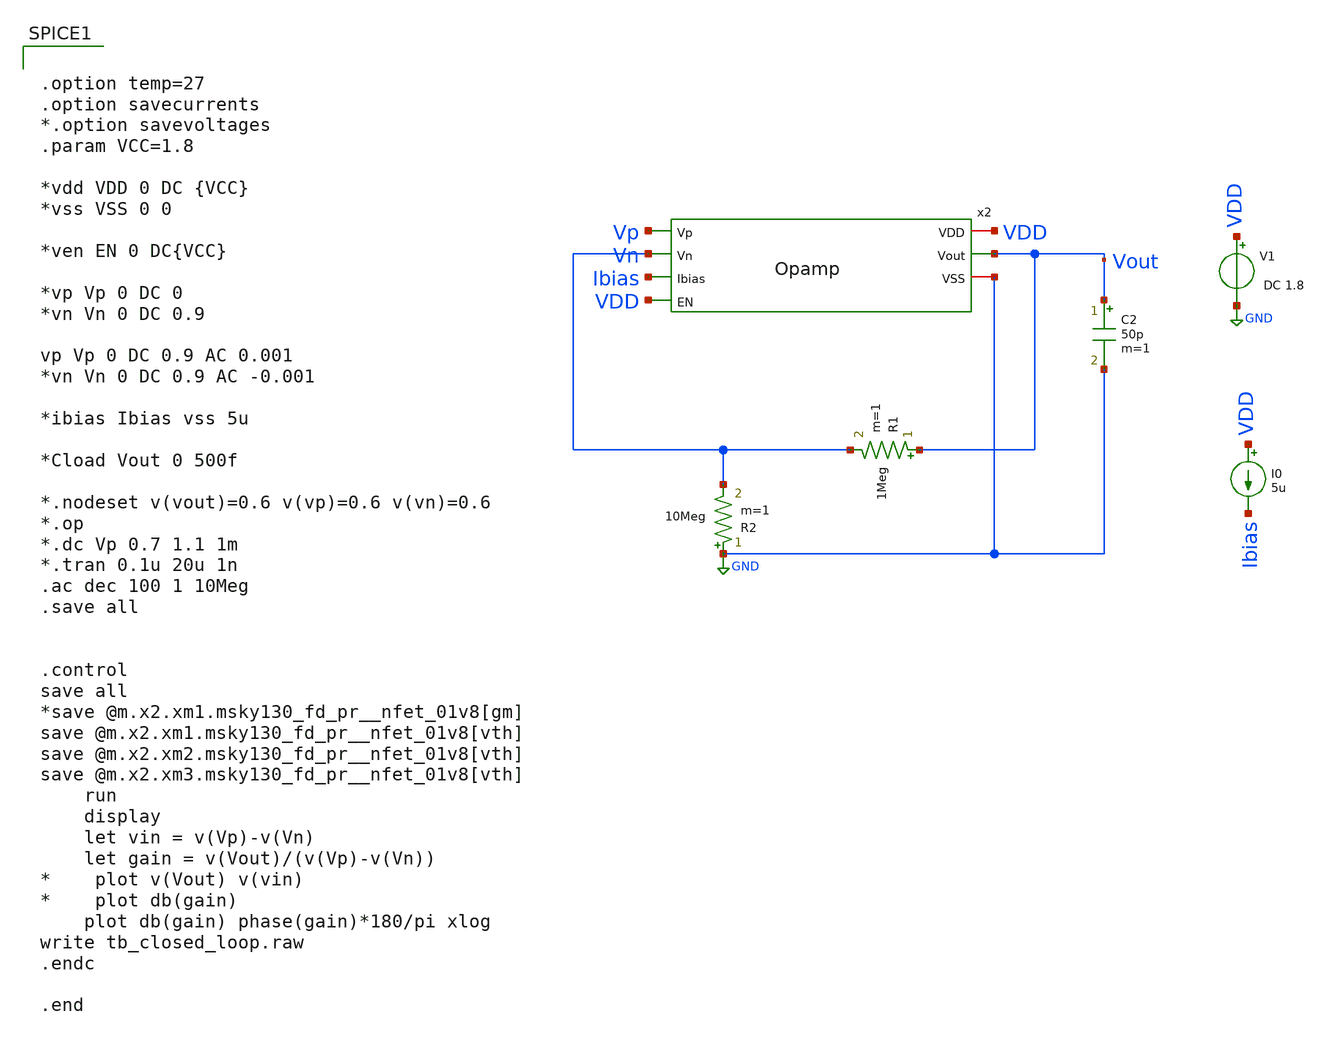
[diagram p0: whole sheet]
** sch_path: xschem/tb_closed_loop.sch
**.subckt tb_closed_loop
R1 Vout Vn 1Meg m=1
V1 VDD GND DC 1.8
I0 VDD Ibias 5u
x2 VDD Vp Vn Vout Ibias GND VDD Opamp
C2 Vout GND 50p m=1
R2 GND Vn 10Meg m=1
**** begin user architecture code


.option temp=27
.option savecurrents
*.option savevoltages
.param VCC=1.8

*vdd VDD 0 DC {VCC}
*vss VSS 0 0

*ven EN 0 DC{VCC}

*vp Vp 0 DC 0
*vn Vn 0 DC 0.9

vp Vp 0 DC 0.9 AC 0.001
*vn Vn 0 DC 0.9 AC -0.001

*ibias Ibias vss 5u

*Cload Vout 0 500f

*.nodeset v(vout)=0.6 v(vp)=0.6 v(vn)=0.6
*.op
*.dc Vp 0.7 1.1 1m
*.tran 0.1u 20u 1n
.ac dec 100 1 10Meg
.save all


.control
save all
*save @m.x2.xm1.msky130_fd_pr__nfet_01v8[gm]
save @m.x2.xm1.msky130_fd_pr__nfet_01v8[vth]
save @m.x2.xm2.msky130_fd_pr__nfet_01v8[vth]
save @m.x2.xm3.msky130_fd_pr__nfet_01v8[vth]
	run
	display
	let vin = v(Vp)-v(Vn)
	let gain = v(Vout)/(v(Vp)-v(Vn))
*	plot v(Vout) v(vin)
*	plot db(gain)
	plot db(gain) phase(gain)*180/pi xlog
write tb_closed_loop.raw
.endc

.end



** opencircuitdesign pdks install
.lib /foss/pdks/sky130A/libs.tech/ngspice/sky130.lib.spice tt


**** end user architecture code
**.ends

* expanding   symbol:  /foss/designs/cmos-two-stage-opamp/xschem/Opamp.sym # of pins=7
** sym_path: xschem/Opamp.sym
** sch_path: xschem/Opamp.sch
.subckt Opamp VDD Vp Vn Vout Ibias VSS EN
*.ipin Vn
*.ipin Ibias
*.ipin Vp
*.ipin EN
*.opin Vout
*.iopin VSS
*.iopin VDD
XM2 Vouts1 Vp Itail GND sky130_fd_pr__nfet_01v8 L=1 W=4 nf=1 ad='int((nf+1)/2) * W/nf * 0.29' as='int((nf+2)/2) * W/nf * 0.29'
+ pd='2*int((nf+1)/2) * (W/nf + 0.29)' ps='2*int((nf+2)/2) * (W/nf + 0.29)' nrd='0.29 / W' nrs='0.29 / W'
+ sa=0 sb=0 sd=0 mult=1 m=1
XM4 Vouts1 net1 VDD VDD sky130_fd_pr__pfet_01v8 L=1 W=8 nf=1 ad='int((nf+1)/2) * W/nf * 0.29' as='int((nf+2)/2) * W/nf * 0.29'
+ pd='2*int((nf+1)/2) * (W/nf + 0.29)' ps='2*int((nf+2)/2) * (W/nf + 0.29)' nrd='0.29 / W' nrs='0.29 / W'
+ sa=0 sb=0 sd=0 mult=1 m=1
XM3 net1 net1 VDD VDD sky130_fd_pr__pfet_01v8 L=1 W=8 nf=1 ad='int((nf+1)/2) * W/nf * 0.29' as='int((nf+2)/2) * W/nf * 0.29'
+ pd='2*int((nf+1)/2) * (W/nf + 0.29)' ps='2*int((nf+2)/2) * (W/nf + 0.29)' nrd='0.29 / W' nrs='0.29 / W'
+ sa=0 sb=0 sd=0 mult=1 m=1
XM1 net1 Vn Itail GND sky130_fd_pr__nfet_01v8 L=1 W=4 nf=1 ad='int((nf+1)/2) * W/nf * 0.29' as='int((nf+2)/2) * W/nf * 0.29'
+ pd='2*int((nf+1)/2) * (W/nf + 0.29)' ps='2*int((nf+2)/2) * (W/nf + 0.29)' nrd='0.29 / W' nrs='0.29 / W'
+ sa=0 sb=0 sd=0 mult=1 m=1
XM6 Vout Vouts1 VDD VDD sky130_fd_pr__pfet_01v8 L=1 W=22 nf=1 ad='int((nf+1)/2) * W/nf * 0.29' as='int((nf+2)/2) * W/nf * 0.29'
+ pd='2*int((nf+1)/2) * (W/nf + 0.29)' ps='2*int((nf+2)/2) * (W/nf + 0.29)' nrd='0.29 / W' nrs='0.29 / W'
+ sa=0 sb=0 sd=0 mult=1 m=1
XM5 Itail Ibias VSS VSS sky130_fd_pr__nfet_01v8 L=2 W=7 nf=4 ad='int((nf+1)/2) * W/nf * 0.29' as='int((nf+2)/2) * W/nf * 0.29'
+ pd='2*int((nf+1)/2) * (W/nf + 0.29)' ps='2*int((nf+2)/2) * (W/nf + 0.29)' nrd='0.29 / W' nrs='0.29 / W'
+ sa=0 sb=0 sd=0 mult=5 m=5
XM7 Vout Ibias VSS VSS sky130_fd_pr__nfet_01v8 L=2 W=7 nf=4 ad='int((nf+1)/2) * W/nf * 0.29' as='int((nf+2)/2) * W/nf * 0.29'
+ pd='2*int((nf+1)/2) * (W/nf + 0.29)' ps='2*int((nf+2)/2) * (W/nf + 0.29)' nrd='0.29 / W' nrs='0.29 / W'
+ sa=0 sb=0 sd=0 mult=6 m=6
XM8 Ibias Ibias VSS VSS sky130_fd_pr__nfet_01v8 L=2 W=7 nf=4 ad='int((nf+1)/2) * W/nf * 0.29' as='int((nf+2)/2) * W/nf * 0.29'
+ pd='2*int((nf+1)/2) * (W/nf + 0.29)' ps='2*int((nf+2)/2) * (W/nf + 0.29)' nrd='0.29 / W' nrs='0.29 / W'
+ sa=0 sb=0 sd=0 mult=1 m=1
XM9 VSS EN Ibias Ibias sky130_fd_pr__pfet_01v8 L=2 W=7 nf=1 ad='int((nf+1)/2) * W/nf * 0.29' as='int((nf+2)/2) * W/nf * 0.29'
+ pd='2*int((nf+1)/2) * (W/nf + 0.29)' ps='2*int((nf+2)/2) * (W/nf + 0.29)' nrd='0.29 / W' nrs='0.29 / W'
+ sa=0 sb=0 sd=0 mult=1 m=1
XM10 VSS EN Ibias Ibias sky130_fd_pr__pfet_01v8 L=1 W=2 nf=1 ad='int((nf+1)/2) * W/nf * 0.29' as='int((nf+2)/2) * W/nf * 0.29'
+ pd='2*int((nf+1)/2) * (W/nf + 0.29)' ps='2*int((nf+2)/2) * (W/nf + 0.29)' nrd='0.29 / W' nrs='0.29 / W'
+ sa=0 sb=0 sd=0 mult=1 m=1
XC2 net2 Vout sky130_fd_pr__cap_mim_m3_1 W=7 L=7 MF=200 m=200
Rz net2 Vouts1 sky130_fd_pr__res_generic_l1 W=1 L=1300 m=1
**** begin user architecture code
"Is Subcircuit" = YES
**** end user architecture code
.ends

.GLOBAL GND
.end
